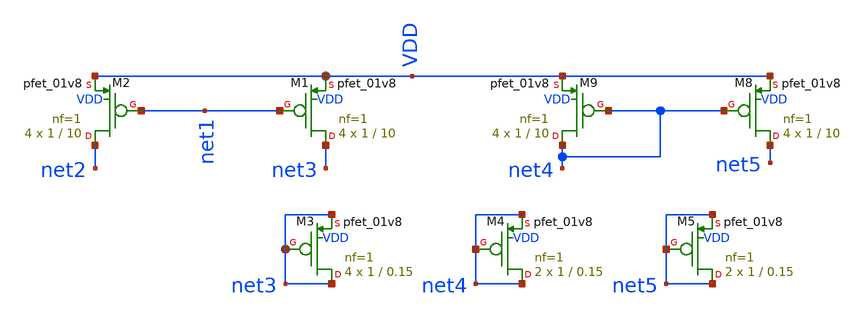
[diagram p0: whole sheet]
** sch_path: magic/pmos_current_source.sch
**.subckt pmos_current_source
XM1 net3 net1 VDD VDD sky130_fd_pr__pfet_01v8 L=10 W=1 nf=1 ad='int((nf+1)/2) * W/nf * 0.29' as='int((nf+2)/2) * W/nf * 0.29'
+ pd='2*int((nf+1)/2) * (W/nf + 0.29)' ps='2*int((nf+2)/2) * (W/nf + 0.29)' nrd='0.29 / W' nrs='0.29 / W'
+ sa=0 sb=0 sd=0 mult=4 m=4
XM2 net2 net1 VDD VDD sky130_fd_pr__pfet_01v8 L=10 W=1 nf=1 ad='int((nf+1)/2) * W/nf * 0.29' as='int((nf+2)/2) * W/nf * 0.29'
+ pd='2*int((nf+1)/2) * (W/nf + 0.29)' ps='2*int((nf+2)/2) * (W/nf + 0.29)' nrd='0.29 / W' nrs='0.29 / W'
+ sa=0 sb=0 sd=0 mult=4 m=4
XM8 net5 net4 VDD VDD sky130_fd_pr__pfet_01v8 L=10 W=1 nf=1 ad='int((nf+1)/2) * W/nf * 0.29' as='int((nf+2)/2) * W/nf * 0.29'
+ pd='2*int((nf+1)/2) * (W/nf + 0.29)' ps='2*int((nf+2)/2) * (W/nf + 0.29)' nrd='0.29 / W' nrs='0.29 / W'
+ sa=0 sb=0 sd=0 mult=4 m=4
XM9 net4 net4 VDD VDD sky130_fd_pr__pfet_01v8 L=10 W=1 nf=1 ad='int((nf+1)/2) * W/nf * 0.29' as='int((nf+2)/2) * W/nf * 0.29'
+ pd='2*int((nf+1)/2) * (W/nf + 0.29)' ps='2*int((nf+2)/2) * (W/nf + 0.29)' nrd='0.29 / W' nrs='0.29 / W'
+ sa=0 sb=0 sd=0 mult=4 m=4
XM3 net3 net3 net3 VDD sky130_fd_pr__pfet_01v8 L=0.15 W=1 nf=1 ad='int((nf+1)/2) * W/nf * 0.29' as='int((nf+2)/2) * W/nf * 0.29'
+ pd='2*int((nf+1)/2) * (W/nf + 0.29)' ps='2*int((nf+2)/2) * (W/nf + 0.29)' nrd='0.29 / W' nrs='0.29 / W'
+ sa=0 sb=0 sd=0 mult=4 m=4
XM4 net4 net4 net4 VDD sky130_fd_pr__pfet_01v8 L=0.15 W=1 nf=1 ad='int((nf+1)/2) * W/nf * 0.29' as='int((nf+2)/2) * W/nf * 0.29'
+ pd='2*int((nf+1)/2) * (W/nf + 0.29)' ps='2*int((nf+2)/2) * (W/nf + 0.29)' nrd='0.29 / W' nrs='0.29 / W'
+ sa=0 sb=0 sd=0 mult=2 m=2
XM5 net5 net5 net5 VDD sky130_fd_pr__pfet_01v8 L=0.15 W=1 nf=1 ad='int((nf+1)/2) * W/nf * 0.29' as='int((nf+2)/2) * W/nf * 0.29'
+ pd='2*int((nf+1)/2) * (W/nf + 0.29)' ps='2*int((nf+2)/2) * (W/nf + 0.29)' nrd='0.29 / W' nrs='0.29 / W'
+ sa=0 sb=0 sd=0 mult=2 m=2
**.ends
.end
